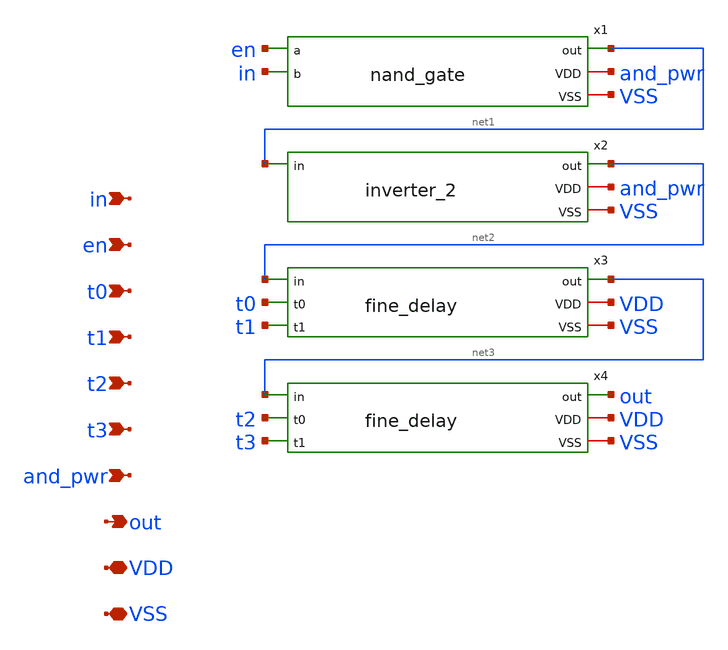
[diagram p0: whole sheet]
** sch_path: xschem/input_stage_andpwr.sch
**.subckt input_stage_andpwr VDD in out VSS t0 t1 t2 t3 en and_pwr
*.iopin VDD
*.ipin in
*.opin out
*.iopin VSS
*.ipin t0
*.ipin t1
*.ipin t2
*.ipin t3
*.ipin en
*.ipin and_pwr
x1 en in net1 and_pwr VSS nand_gate
x2 net1 net2 and_pwr VSS inverter_2
x3 net2 t0 t1 net3 VDD VSS fine_delay
x4 net3 t2 t3 out VDD VSS fine_delay
**.ends

* expanding   symbol:  nand_gate.sym # of pins=5
** sym_path: xschem/nand_gate.sym
** sch_path: xschem/nand_gate.sch
.subckt nand_gate a b out VDD VSS
*.iopin VDD
*.ipin a
*.opin out
*.iopin VSS
*.ipin b
XM7 out a net1 VSS sky130_fd_pr__nfet_01v8 L=0.15 W=2 nf=1 ad='int((nf+1)/2) * W/nf * 0.29' as='int((nf+2)/2) * W/nf * 0.29'
+ pd='2*int((nf+1)/2) * (W/nf + 0.29)' ps='2*int((nf+2)/2) * (W/nf + 0.29)' nrd='0.29 / W' nrs='0.29 / W'
+ sa=0 sb=0 sd=0 mult=1 m=1
XM1 out a VDD VDD sky130_fd_pr__pfet_01v8 L=0.15 W=3 nf=1 ad='int((nf+1)/2) * W/nf * 0.29' as='int((nf+2)/2) * W/nf * 0.29'
+ pd='2*int((nf+1)/2) * (W/nf + 0.29)' ps='2*int((nf+2)/2) * (W/nf + 0.29)' nrd='0.29 / W' nrs='0.29 / W'
+ sa=0 sb=0 sd=0 mult=1 m=1
XM2 net1 b VSS VSS sky130_fd_pr__nfet_01v8 L=0.15 W=2 nf=1 ad='int((nf+1)/2) * W/nf * 0.29' as='int((nf+2)/2) * W/nf * 0.29'
+ pd='2*int((nf+1)/2) * (W/nf + 0.29)' ps='2*int((nf+2)/2) * (W/nf + 0.29)' nrd='0.29 / W' nrs='0.29 / W'
+ sa=0 sb=0 sd=0 mult=1 m=1
XM3 out b VDD VDD sky130_fd_pr__pfet_01v8 L=0.15 W=3 nf=1 ad='int((nf+1)/2) * W/nf * 0.29' as='int((nf+2)/2) * W/nf * 0.29'
+ pd='2*int((nf+1)/2) * (W/nf + 0.29)' ps='2*int((nf+2)/2) * (W/nf + 0.29)' nrd='0.29 / W' nrs='0.29 / W'
+ sa=0 sb=0 sd=0 mult=1 m=1
.ends


* expanding   symbol:  inverter_2.sym # of pins=4
** sym_path: xschem/inverter_2.sym
** sch_path: xschem/inverter_2.sch
.subckt inverter_2 in out VDD VSS
*.iopin VDD
*.ipin in
*.opin out
*.iopin VSS
XM1 out in VDD VDD sky130_fd_pr__pfet_01v8 L=0.15 W=3 nf=1 ad='int((nf+1)/2) * W/nf * 0.29' as='int((nf+2)/2) * W/nf * 0.29'
+ pd='2*int((nf+1)/2) * (W/nf + 0.29)' ps='2*int((nf+2)/2) * (W/nf + 0.29)' nrd='0.29 / W' nrs='0.29 / W'
+ sa=0 sb=0 sd=0 mult=1 m=1
XM2 out in VSS VSS sky130_fd_pr__nfet_01v8 L=0.15 W=1 nf=1 ad='int((nf+1)/2) * W/nf * 0.29' as='int((nf+2)/2) * W/nf * 0.29'
+ pd='2*int((nf+1)/2) * (W/nf + 0.29)' ps='2*int((nf+2)/2) * (W/nf + 0.29)' nrd='0.29 / W' nrs='0.29 / W'
+ sa=0 sb=0 sd=0 mult=1 m=1
.ends


* expanding   symbol:  fine_delay.sym # of pins=6
** sym_path: xschem/fine_delay.sym
** sch_path: xschem/fine_delay.sch
.subckt fine_delay in t0 t1 out VDD VSS
*.iopin VDD
*.ipin in
*.opin out
*.iopin VSS
*.ipin t0
*.ipin t1
XM1 net1 in VDD VDD sky130_fd_pr__pfet_01v8 L=0.15 W=3 nf=1 ad='int((nf+1)/2) * W/nf * 0.29' as='int((nf+2)/2) * W/nf * 0.29'
+ pd='2*int((nf+1)/2) * (W/nf + 0.29)' ps='2*int((nf+2)/2) * (W/nf + 0.29)' nrd='0.29 / W' nrs='0.29 / W'
+ sa=0 sb=0 sd=0 mult=1 m=1
XM2 net3 in VSS VSS sky130_fd_pr__nfet_01v8 L=0.15 W=1 nf=1 ad='int((nf+1)/2) * W/nf * 0.29' as='int((nf+2)/2) * W/nf * 0.29'
+ pd='2*int((nf+1)/2) * (W/nf + 0.29)' ps='2*int((nf+2)/2) * (W/nf + 0.29)' nrd='0.29 / W' nrs='0.29 / W'
+ sa=0 sb=0 sd=0 mult=1 m=1
XM5 net3 t1 VSS VSS sky130_fd_pr__nfet_01v8 L=0.15 W=2 nf=1 ad='int((nf+1)/2) * W/nf * 0.29' as='int((nf+2)/2) * W/nf * 0.29'
+ pd='2*int((nf+1)/2) * (W/nf + 0.29)' ps='2*int((nf+2)/2) * (W/nf + 0.29)' nrd='0.29 / W' nrs='0.29 / W'
+ sa=0 sb=0 sd=0 mult=1 m=1
XM8 out net1 VDD VDD sky130_fd_pr__pfet_01v8 L=0.15 W=3 nf=1 ad='int((nf+1)/2) * W/nf * 0.29' as='int((nf+2)/2) * W/nf * 0.29'
+ pd='2*int((nf+1)/2) * (W/nf + 0.29)' ps='2*int((nf+2)/2) * (W/nf + 0.29)' nrd='0.29 / W' nrs='0.29 / W'
+ sa=0 sb=0 sd=0 mult=1 m=1
XM9 out net1 VSS VSS sky130_fd_pr__nfet_01v8 L=0.15 W=1 nf=1 ad='int((nf+1)/2) * W/nf * 0.29' as='int((nf+2)/2) * W/nf * 0.29'
+ pd='2*int((nf+1)/2) * (W/nf + 0.29)' ps='2*int((nf+2)/2) * (W/nf + 0.29)' nrd='0.29 / W' nrs='0.29 / W'
+ sa=0 sb=0 sd=0 mult=1 m=1
XM10 net2 in net3 VSS sky130_fd_pr__nfet_01v8 L=0.15 W=1 nf=1 ad='int((nf+1)/2) * W/nf * 0.29' as='int((nf+2)/2) * W/nf * 0.29'
+ pd='2*int((nf+1)/2) * (W/nf + 0.29)' ps='2*int((nf+2)/2) * (W/nf + 0.29)' nrd='0.29 / W' nrs='0.29 / W'
+ sa=0 sb=0 sd=0 mult=1 m=1
XM11 net2 t0 net3 VSS sky130_fd_pr__nfet_01v8 L=0.15 W=2 nf=1 ad='int((nf+1)/2) * W/nf * 0.29' as='int((nf+2)/2) * W/nf * 0.29'
+ pd='2*int((nf+1)/2) * (W/nf + 0.29)' ps='2*int((nf+2)/2) * (W/nf + 0.29)' nrd='0.29 / W' nrs='0.29 / W'
+ sa=0 sb=0 sd=0 mult=1 m=1
XM3 net1 in net2 VSS sky130_fd_pr__nfet_01v8 L=0.15 W=1 nf=1 ad='int((nf+1)/2) * W/nf * 0.29' as='int((nf+2)/2) * W/nf * 0.29'
+ pd='2*int((nf+1)/2) * (W/nf + 0.29)' ps='2*int((nf+2)/2) * (W/nf + 0.29)' nrd='0.29 / W' nrs='0.29 / W'
+ sa=0 sb=0 sd=0 mult=1 m=1
XM4 net1 in net2 VSS sky130_fd_pr__nfet_01v8 L=0.15 W=1 nf=1 ad='int((nf+1)/2) * W/nf * 0.29' as='int((nf+2)/2) * W/nf * 0.29'
+ pd='2*int((nf+1)/2) * (W/nf + 0.29)' ps='2*int((nf+2)/2) * (W/nf + 0.29)' nrd='0.29 / W' nrs='0.29 / W'
+ sa=0 sb=0 sd=0 mult=1 m=1
XM6 net1 in net2 VSS sky130_fd_pr__nfet_01v8 L=0.15 W=1 nf=1 ad='int((nf+1)/2) * W/nf * 0.29' as='int((nf+2)/2) * W/nf * 0.29'
+ pd='2*int((nf+1)/2) * (W/nf + 0.29)' ps='2*int((nf+2)/2) * (W/nf + 0.29)' nrd='0.29 / W' nrs='0.29 / W'
+ sa=0 sb=0 sd=0 mult=1 m=1
.ends

.end
